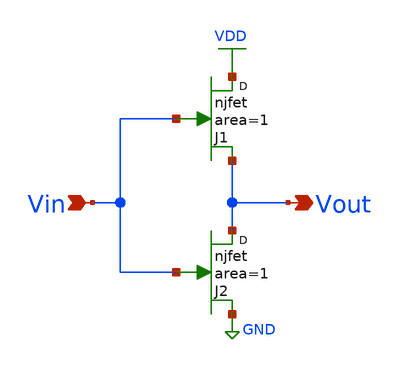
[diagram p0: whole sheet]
** sch_path: analog/xschem/schematics/inveter.sch
**.subckt inveter Vin Vout
*.ipin Vin
*.opin Vout
J1 VDD Vin Vout njfet area=1 m=1
J2 Vout Vin GND njfet area=1 m=1
**.ends
.GLOBAL VDD
.GLOBAL GND
.end
